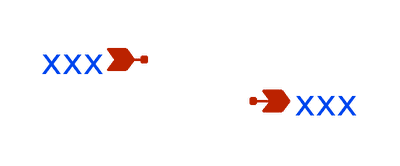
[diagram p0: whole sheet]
** sch_path: xschem/lib/d_fa_ext.sch
**.subckt d_fa_ext xxx xxx
*.ipin xxx
*.opin xxx
**** begin user architecture code


.subckt phase_extractor sink_out p4 p3 p2 p1 p0 pn4 pn3 pn2 pn1 pn0
a_ext_and0 [p0 pn1_b] ext0 and1
a_ext_and1 [p1 pn2_b] ext1 and1
a_ext_and2 [p2 pn3_b] ext2 and1
a_ext_and3 [p3 pn4_b] ext3 and1
a_ext_and4 [p4 pn0_b] ext4 and1

a_ext_inv0 pn1 pn1_b inv1
a_ext_inv1 pn2 pn2_b inv1
a_ext_inv2 pn3 pn3_b inv1
a_ext_inv3 pn4 pn4_b inv1
a_ext_inv4 pn0 pn0_b inv1

a_ext_or0 [ext2 ext3] net3 or1
a_ext_or1 [ext0 ext1] net4 or1
a_ext_or2 [ext4 GND ]  net5 or1
a_ext_or3 [net5 GND ]  net6 or1
a_ext_or4 [net4 net3] net7 or1
a_ext_or5 [net7 net6] sink_out or1

.model and1 d_and(rise_delay = 0.5e-9 fall_delay = 0.3e-9 input_load = 0.5e-12)
.model inv1 d_inverter(rise_delay = 0.5e-9 fall_delay = 0.3e-9 input_load = 0.5e-12)
.model or1 d_or(rise_delay = 0.5e-9 fall_delay = 0.3e-9 input_load = 0.5e-12)

.ends

*** adc_bridge blocks ***
aconverter [p0 p1 p2 p3 p4 pn0 pn1 pn2 pn3 pn4] [d_p0 d_p1 d_p2 d_p3 d_p4 d_pn0 d_pn1 d_pn2 d_pn3
+ d_pn4] adc1
.model adc1 adc_bridge (in_low='v_dd/2-5m' in_high='v_dd/2+5m' rise_delay=1.0e-12 fall_delay=1.0e-12)


**** end user architecture code
**.ends
.end
